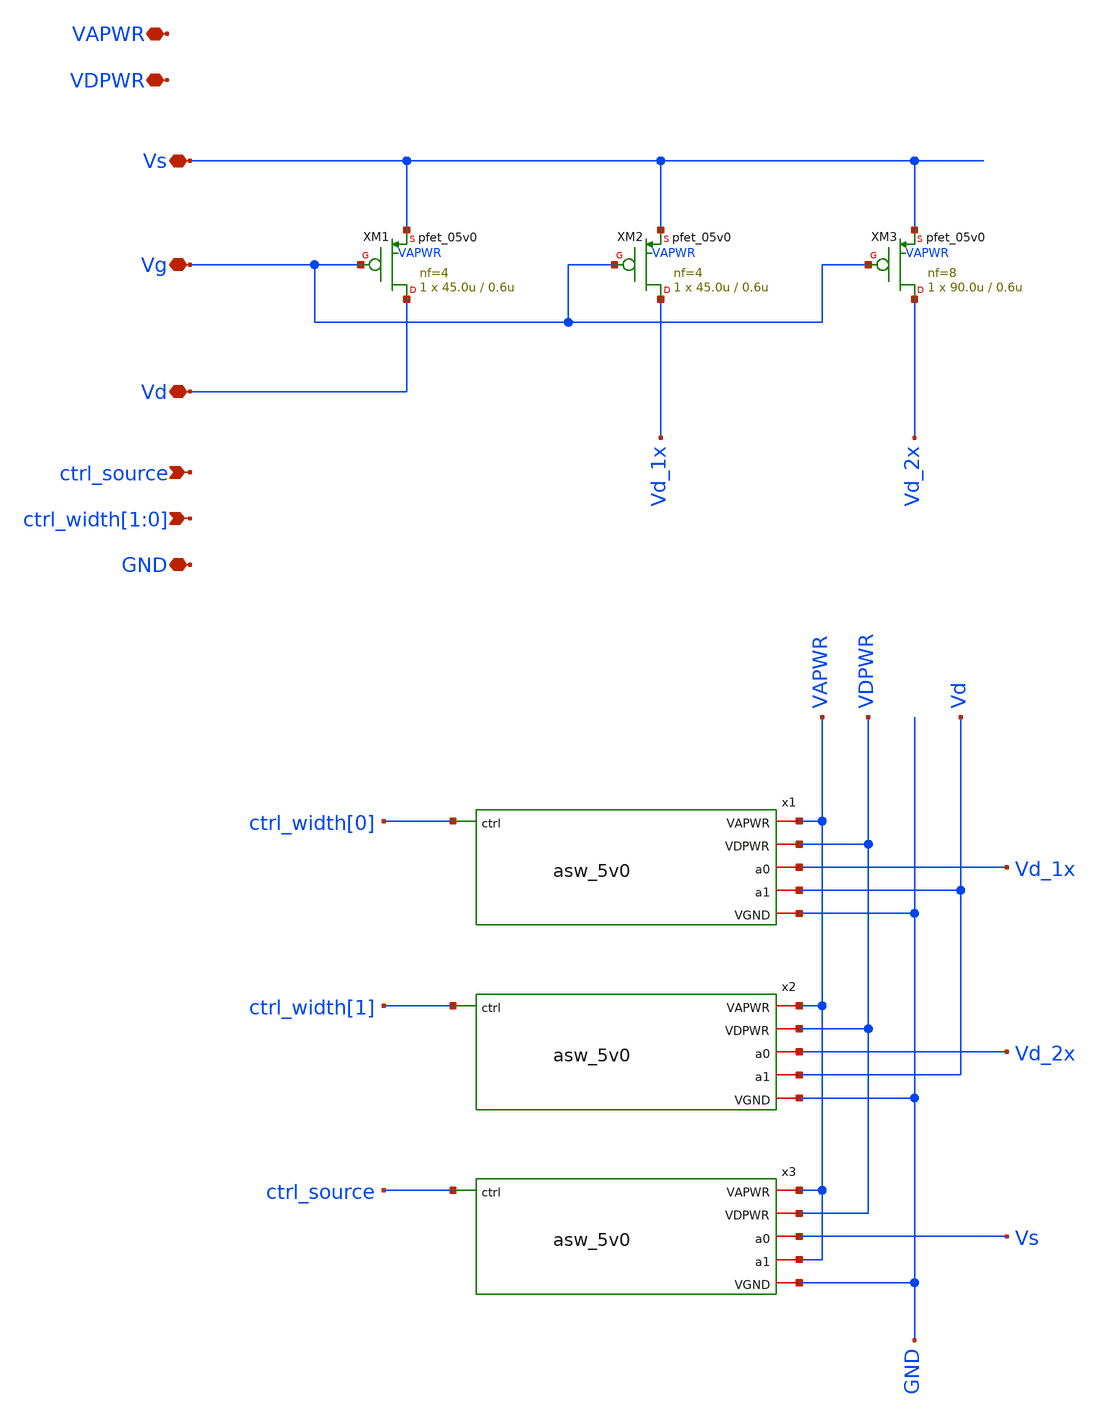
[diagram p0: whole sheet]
** sch_path: xschem/pmos_prog.sch
**.subckt pmos_prog ctrl_width[1],ctrl_width[0] Vs Vg Vd VAPWR VDPWR GND ctrl_source
*.ipin ctrl_width[1],ctrl_width[0]
*.iopin Vs
*.iopin Vg
*.iopin Vd
*.iopin VAPWR
*.iopin VDPWR
*.iopin GND
*.ipin ctrl_source
x1 GND VDPWR VAPWR ctrl_width[0] Vd_1x Vd asw_5v0
x2 GND VDPWR VAPWR ctrl_width[1] Vd_2x Vd asw_5v0
x3 GND VDPWR VAPWR ctrl_source Vs VAPWR asw_5v0
XM1 Vd Vg Vs VAPWR pfet_05v0 L=0.6u W=45.0u nf=4 ad='int((nf+1)/2) * W/nf * 0.18u' as='int((nf+2)/2) * W/nf * 0.18u'
+ pd='2*int((nf+1)/2) * (W/nf + 0.18u)' ps='2*int((nf+2)/2) * (W/nf + 0.18u)' nrd='0.18u / W' nrs='0.18u / W'
+ sa=0 sb=0 sd=0 m=1 par=1
XM2 Vd_1x Vg Vs VAPWR pfet_05v0 L=0.6u W=45.0u nf=4 ad='int((nf+1)/2) * W/nf * 0.18u' as='int((nf+2)/2) * W/nf * 0.18u'
+ pd='2*int((nf+1)/2) * (W/nf + 0.18u)' ps='2*int((nf+2)/2) * (W/nf + 0.18u)' nrd='0.18u / W' nrs='0.18u / W'
+ sa=0 sb=0 sd=0 m=1 par=1
XM3 Vd_2x Vg Vs VAPWR pfet_05v0 L=0.6u W=90.0u nf=8 ad='int((nf+1)/2) * W/nf * 0.18u' as='int((nf+2)/2) * W/nf * 0.18u'
+ pd='2*int((nf+1)/2) * (W/nf + 0.18u)' ps='2*int((nf+2)/2) * (W/nf + 0.18u)' nrd='0.18u / W' nrs='0.18u / W'
+ sa=0 sb=0 sd=0 m=1 par=1
**.ends

* expanding   symbol:  asw_5v0.sym # of pins=6
** sym_path: xschem/asw_5v0.sym
** sch_path: xschem/asw_5v0.sch
.subckt asw_5v0 VGND VDPWR VAPWR ctrl a0 a1
*.ipin ctrl
*.iopin VDPWR
*.iopin VGND
*.iopin a0
*.iopin VAPWR
*.iopin a1
x1 VGND VDPWR VAPWR ctrl tgon_p tgon_n lv2hv
XM1 a0 tgon_n a1 VAPWR pfet_05v0 L=0.50u W=592u nf=16 ad='int((nf+1)/2) * W/nf * 0.18u' as='int((nf+2)/2) * W/nf * 0.18u'
+ pd='2*int((nf+1)/2) * (W/nf + 0.18u)' ps='2*int((nf+2)/2) * (W/nf + 0.18u)' nrd='0.18u / W' nrs='0.18u / W'
+ sa=0 sb=0 sd=0 m=1 par=1
XM2 a1 tgon_p a0 VGND nfet_05v0 L=0.60u W=248u nf=8 ad='int((nf+1)/2) * W/nf * 0.18u' as='int((nf+2)/2) * W/nf * 0.18u'
+ pd='2*int((nf+1)/2) * (W/nf + 0.18u)' ps='2*int((nf+2)/2) * (W/nf + 0.18u)' nrd='0.18u / W' nrs='0.18u / W'
+ sa=0 sb=0 sd=0 m=1 par=1
.ends


* expanding   symbol:  lv2hv.sym # of pins=6
** sym_path: lv2hv.sym
** sch_path: lv2hv.sch
.subckt lv2hv VGND VDPWR VAPWR in out_p out_n
*.iopin VAPWR
*.iopin VGND
*.ipin in
*.iopin VDPWR
*.opin out_p
*.opin out_n
XM1 in_n in VGND VGND nfet_03v3 L=0.28u W=0.89u nf=1 ad='int((nf+1)/2) * W/nf * 0.18u' as='int((nf+2)/2) * W/nf * 0.18u'
+ pd='2*int((nf+1)/2) * (W/nf + 0.18u)' ps='2*int((nf+2)/2) * (W/nf + 0.18u)' nrd='0.18u / W' nrs='0.18u / W'
+ sa=0 sb=0 sd=0 m=1 par=1
XM2 in_n in VDPWR VDPWR pfet_03v3 L=0.28u W=2.0u nf=1 ad='int((nf+1)/2) * W/nf * 0.18u' as='int((nf+2)/2) * W/nf * 0.18u'
+ pd='2*int((nf+1)/2) * (W/nf + 0.18u)' ps='2*int((nf+2)/2) * (W/nf + 0.18u)' nrd='0.18u / W' nrs='0.18u / W'
+ sa=0 sb=0 sd=0 m=1 par=1
XM3 VGND in_p net1 VGND nfet_05v0 L=0.6u W=0.5u nf=1 ad='int((nf+1)/2) * W/nf * 0.18u' as='int((nf+2)/2) * W/nf * 0.18u'
+ pd='2*int((nf+1)/2) * (W/nf + 0.18u)' ps='2*int((nf+2)/2) * (W/nf + 0.18u)' nrd='0.18u / W' nrs='0.18u / W'
+ sa=0 sb=0 sd=0 m=1 par=1
XM4 net1 net2 VAPWR VAPWR pfet_05v0 L=0.5u W=0.5u nf=1 ad='int((nf+1)/2) * W/nf * 0.18u' as='int((nf+2)/2) * W/nf * 0.18u'
+ pd='2*int((nf+1)/2) * (W/nf + 0.18u)' ps='2*int((nf+2)/2) * (W/nf + 0.18u)' nrd='0.18u / W' nrs='0.18u / W'
+ sa=0 sb=0 sd=0 m=1 par=1
XM5 net2 in_n VGND VGND nfet_05v0 L=0.6u W=0.5u nf=1 ad='int((nf+1)/2) * W/nf * 0.18u' as='int((nf+2)/2) * W/nf * 0.18u'
+ pd='2*int((nf+1)/2) * (W/nf + 0.18u)' ps='2*int((nf+2)/2) * (W/nf + 0.18u)' nrd='0.18u / W' nrs='0.18u / W'
+ sa=0 sb=0 sd=0 m=1 par=1
XM6 net2 net1 VAPWR VAPWR pfet_05v0 L=0.5u W=0.5u nf=1 ad='int((nf+1)/2) * W/nf * 0.18u' as='int((nf+2)/2) * W/nf * 0.18u'
+ pd='2*int((nf+1)/2) * (W/nf + 0.18u)' ps='2*int((nf+2)/2) * (W/nf + 0.18u)' nrd='0.18u / W' nrs='0.18u / W'
+ sa=0 sb=0 sd=0 m=1 par=1
XM7 VGND net2 out_n VGND nfet_05v0 L=0.60u W=0.5u nf=1 ad='int((nf+1)/2) * W/nf * 0.18u' as='int((nf+2)/2) * W/nf * 0.18u'
+ pd='2*int((nf+1)/2) * (W/nf + 0.18u)' ps='2*int((nf+2)/2) * (W/nf + 0.18u)' nrd='0.18u / W' nrs='0.18u / W'
+ sa=0 sb=0 sd=0 m=1 par=1
XM8 out_n net2 VAPWR VAPWR pfet_05v0 L=0.5u W=1.0u nf=2 ad='int((nf+1)/2) * W/nf * 0.18u' as='int((nf+2)/2) * W/nf * 0.18u'
+ pd='2*int((nf+1)/2) * (W/nf + 0.18u)' ps='2*int((nf+2)/2) * (W/nf + 0.18u)' nrd='0.18u / W' nrs='0.18u / W'
+ sa=0 sb=0 sd=0 m=1 par=1
XM9 VGND net1 out_p VGND nfet_05v0 L=0.60u W=0.5u nf=1 ad='int((nf+1)/2) * W/nf * 0.18u' as='int((nf+2)/2) * W/nf * 0.18u'
+ pd='2*int((nf+1)/2) * (W/nf + 0.18u)' ps='2*int((nf+2)/2) * (W/nf + 0.18u)' nrd='0.18u / W' nrs='0.18u / W'
+ sa=0 sb=0 sd=0 m=1 par=1
XM10 out_p net1 VAPWR VAPWR pfet_05v0 L=0.5u W=1.0u nf=2 ad='int((nf+1)/2) * W/nf * 0.18u' as='int((nf+2)/2) * W/nf * 0.18u'
+ pd='2*int((nf+1)/2) * (W/nf + 0.18u)' ps='2*int((nf+2)/2) * (W/nf + 0.18u)' nrd='0.18u / W' nrs='0.18u / W'
+ sa=0 sb=0 sd=0 m=1 par=1
XM11 in_p in_n VGND VGND nfet_03v3 L=0.28u W=0.89u nf=1 ad='int((nf+1)/2) * W/nf * 0.18u' as='int((nf+2)/2) * W/nf * 0.18u'
+ pd='2*int((nf+1)/2) * (W/nf + 0.18u)' ps='2*int((nf+2)/2) * (W/nf + 0.18u)' nrd='0.18u / W' nrs='0.18u / W'
+ sa=0 sb=0 sd=0 m=1 par=1
XM12 in_p in_n VDPWR VDPWR pfet_03v3 L=0.28u W=2.0u nf=1 ad='int((nf+1)/2) * W/nf * 0.18u' as='int((nf+2)/2) * W/nf * 0.18u'
+ pd='2*int((nf+1)/2) * (W/nf + 0.18u)' ps='2*int((nf+2)/2) * (W/nf + 0.18u)' nrd='0.18u / W' nrs='0.18u / W'
+ sa=0 sb=0 sd=0 m=1 par=1
.ends

.end
